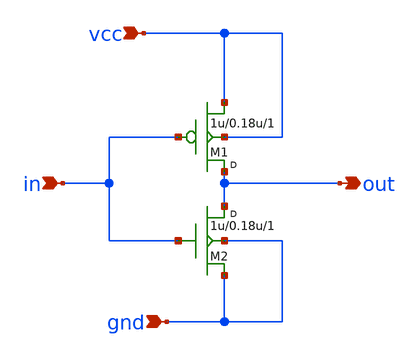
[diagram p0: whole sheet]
** sch_path: xschem/osu_soc_tsmc018/inverter/invx1.sch
**.subckt invx1 in out vcc gnd
*.ipin in
*.opin out
*.ipin vcc
*.ipin gnd
M1 out in vcc vcc pfet w=1u l=0.18u m=1
M2 out in gnd gnd nfet w=1u l=0.18u m=1
**.ends
.end
